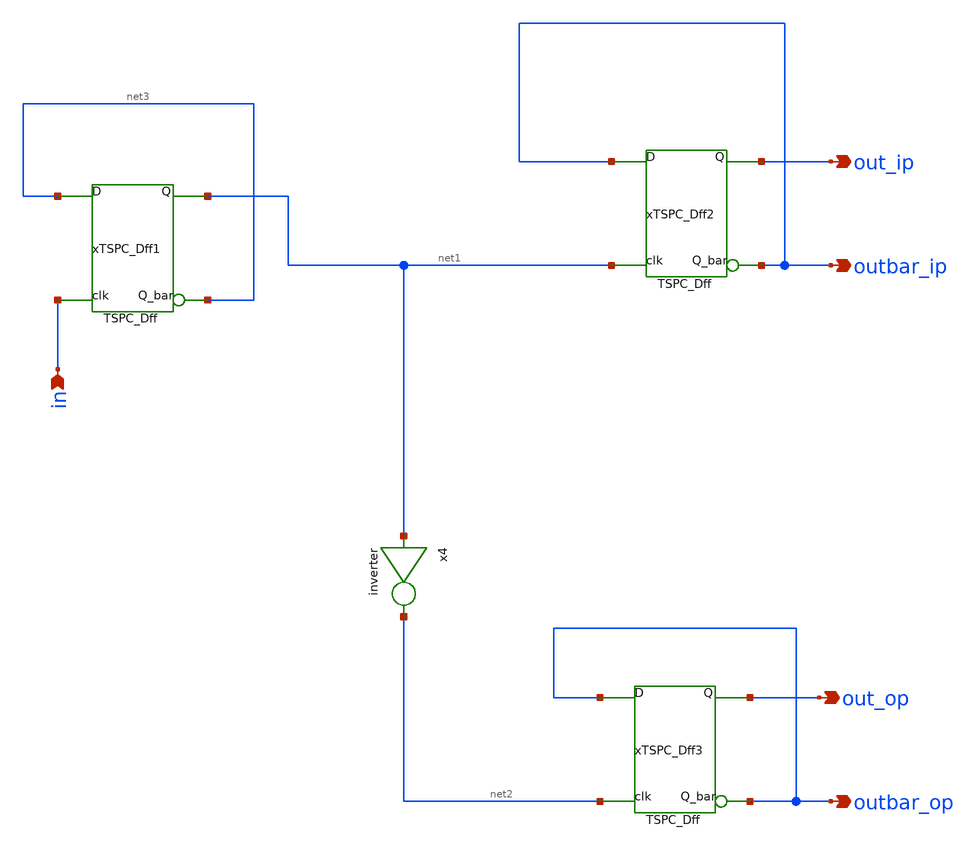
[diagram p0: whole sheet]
** sch_path: Byfour.sch
**.subckt Byfour out_ip out_op outbar_op outbar_ip in
*.opin out_ip
*.opin out_op
*.opin outbar_op
*.opin outbar_ip
*.ipin in
x4 net1 net2 inverter
xTSPC_Dff1 in net3 net3 net1 TSPC_Dff
xTSPC_Dff2 net1 outbar_ip outbar_ip out_ip TSPC_Dff
xTSPC_Dff3 net2 outbar_op outbar_op out_op TSPC_Dff
**.ends

* expanding   symbol:  /home/cegrahul/Desktop/SSCS/inverter.sym # of pins=2
** sym_path: inverter.sym
** sch_path: inverter.sch
.subckt inverter vin vout
*.ipin vin
*.opin vout
XM2 vout vin net1 net1 sky130_fd_pr__pfet_01v8 L=0.15 W=1.68 nf=1 ad='int((nf+1)/2) * W/nf * 0.29' as='int((nf+2)/2) * W/nf * 0.29'
+ pd='2*int((nf+1)/2) * (W/nf + 0.29)' ps='2*int((nf+2)/2) * (W/nf + 0.29)' nrd='0.29 / W' nrs='0.29 / W'
+ sa=0 sb=0 sd=0 mult=1 m=1
XM3 vout vin GND GND sky130_fd_pr__nfet_01v8 L=0.15 W=0.36 nf=1 ad='int((nf+1)/2) * W/nf * 0.29' as='int((nf+2)/2) * W/nf * 0.29'
+ pd='2*int((nf+1)/2) * (W/nf + 0.29)' ps='2*int((nf+2)/2) * (W/nf + 0.29)' nrd='0.29 / W' nrs='0.29 / W'
+ sa=0 sb=0 sd=0 mult=1 m=1
V3 net1 GND 1.8
.ends


* expanding   symbol:  /home/cegrahul/Downloads/TSPC_Dff.sym # of pins=4
** sym_path: TSPC_Dff.sym
** sch_path: TSPC_Dff.sch
.subckt TSPC_Dff CLK D QB Q
*.ipin D
*.ipin CLK
*.opin Q
*.opin QB
V1 VDD GND 1.8
XM3 voutfirst D GND GND sky130_fd_pr__nfet_01v8 L=0.15 W=0.36 nf=1 ad='int((nf+1)/2) * W/nf * 0.29' as='int((nf+2)/2) * W/nf * 0.29'
+ pd='2*int((nf+1)/2) * (W/nf + 0.29)' ps='2*int((nf+2)/2) * (W/nf + 0.29)' nrd='0.29 / W' nrs='0.29 / W'
+ sa=0 sb=0 sd=0 mult=1 m=1
XM4 net1 D VDD VDD sky130_fd_pr__pfet_01v8 L=0.15 W=1.68 nf=1 ad='int((nf+1)/2) * W/nf * 0.29' as='int((nf+2)/2) * W/nf * 0.29'
+ pd='2*int((nf+1)/2) * (W/nf + 0.29)' ps='2*int((nf+2)/2) * (W/nf + 0.29)' nrd='0.29 / W' nrs='0.29 / W'
+ sa=0 sb=0 sd=0 mult=1 m=1
XM5 voutfirst CLK net1 VDD sky130_fd_pr__pfet_01v8 L=0.15 W=1.68 nf=1 ad='int((nf+1)/2) * W/nf * 0.29'
+ as='int((nf+2)/2) * W/nf * 0.29' pd='2*int((nf+1)/2) * (W/nf + 0.29)' ps='2*int((nf+2)/2) * (W/nf + 0.29)'
+ nrd='0.29 / W' nrs='0.29 / W' sa=0 sb=0 sd=0 mult=1 m=1
XM1 net3 CLK GND GND sky130_fd_pr__nfet_01v8 L=0.15 W=0.36 nf=1 ad='int((nf+1)/2) * W/nf * 0.29' as='int((nf+2)/2) * W/nf * 0.29'
+ pd='2*int((nf+1)/2) * (W/nf + 0.29)' ps='2*int((nf+2)/2) * (W/nf + 0.29)' nrd='0.29 / W' nrs='0.29 / W'
+ sa=0 sb=0 sd=0 mult=1 m=1
XM2 net2 CLK VDD VDD sky130_fd_pr__pfet_01v8 L=0.15 W=1.68 nf=1 ad='int((nf+1)/2) * W/nf * 0.29' as='int((nf+2)/2) * W/nf * 0.29'
+ pd='2*int((nf+1)/2) * (W/nf + 0.29)' ps='2*int((nf+2)/2) * (W/nf + 0.29)' nrd='0.29 / W' nrs='0.29 / W'
+ sa=0 sb=0 sd=0 mult=1 m=1
XM6 net2 voutfirst net3 GND sky130_fd_pr__nfet_01v8 L=0.15 W=0.36 nf=1 ad='int((nf+1)/2) * W/nf * 0.29'
+ as='int((nf+2)/2) * W/nf * 0.29' pd='2*int((nf+1)/2) * (W/nf + 0.29)' ps='2*int((nf+2)/2) * (W/nf + 0.29)'
+ nrd='0.29 / W' nrs='0.29 / W' sa=0 sb=0 sd=0 mult=1 m=1
XM7 net4 net2 GND GND sky130_fd_pr__nfet_01v8 L=2 W=0.42 nf=1 ad='int((nf+1)/2) * W/nf * 0.29' as='int((nf+2)/2) * W/nf * 0.29'
+ pd='2*int((nf+1)/2) * (W/nf + 0.29)' ps='2*int((nf+2)/2) * (W/nf + 0.29)' nrd='0.29 / W' nrs='0.29 / W'
+ sa=0 sb=0 sd=0 mult=1 m=1
XM8 voutthird net2 VDD VDD sky130_fd_pr__pfet_01v8 L=0.15 W=1.68 nf=1 ad='int((nf+1)/2) * W/nf * 0.29'
+ as='int((nf+2)/2) * W/nf * 0.29' pd='2*int((nf+1)/2) * (W/nf + 0.29)' ps='2*int((nf+2)/2) * (W/nf + 0.29)'
+ nrd='0.29 / W' nrs='0.29 / W' sa=0 sb=0 sd=0 mult=1 m=1
XM9 voutthird CLK net4 GND sky130_fd_pr__nfet_01v8 L=2 W=0.42 nf=1 ad='int((nf+1)/2) * W/nf * 0.29' as='int((nf+2)/2) * W/nf * 0.29'
+ pd='2*int((nf+1)/2) * (W/nf + 0.29)' ps='2*int((nf+2)/2) * (W/nf + 0.29)' nrd='0.29 / W' nrs='0.29 / W'
+ sa=0 sb=0 sd=0 mult=1 m=1
x1 voutthird Q inverter
x2 Q QB inverter
.ends

.GLOBAL GND
.end
